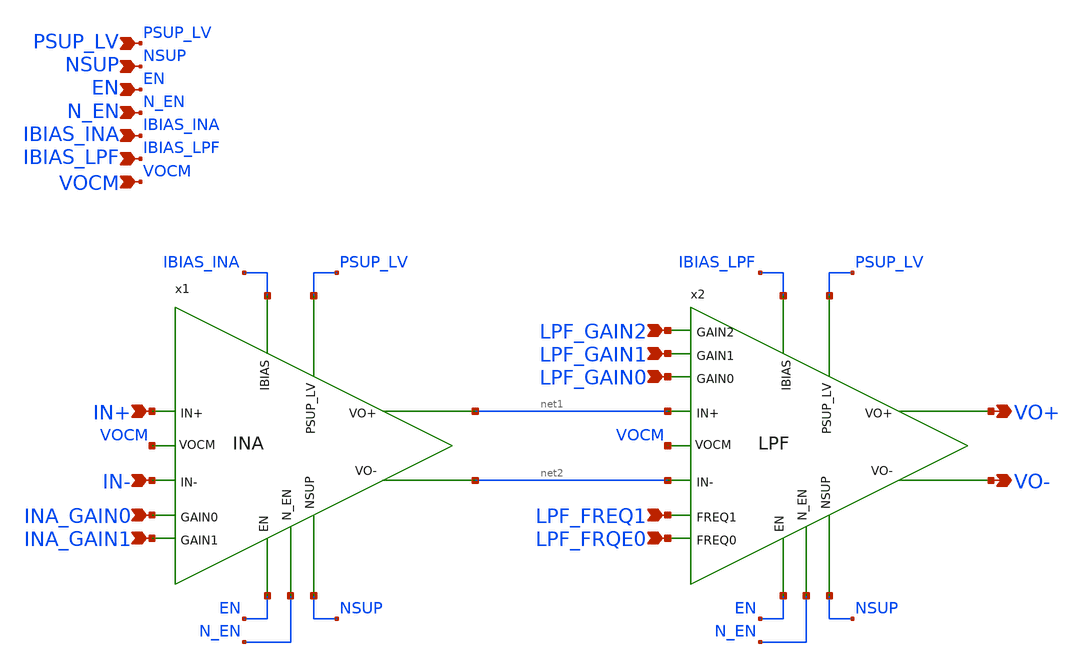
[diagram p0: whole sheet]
** sch_path: xschem/top.sch
**.subckt top IN+ IN- EN N_EN NSUP PSUP_LV IBIAS_INA VOCM VO+ VO- LPF_GAIN2 LPF_GAIN1 LPF_GAIN0
*+ LPF_FREQ1 LPF_FRQE0 INA_GAIN1 INA_GAIN0 IBIAS_LPF
*.ipin IN+
*.ipin IN-
*.ipin EN
*.ipin N_EN
*.ipin NSUP
*.ipin PSUP_LV
*.ipin IBIAS_INA
*.ipin VOCM
*.opin VO+
*.opin VO-
*.ipin LPF_GAIN2
*.ipin LPF_GAIN1
*.ipin LPF_GAIN0
*.ipin LPF_FREQ1
*.ipin LPF_FRQE0
*.ipin INA_GAIN1
*.ipin INA_GAIN0
*.ipin IBIAS_LPF
x2 PSUP_LV NSUP EN N_EN IBIAS_LPF LPF_GAIN2 LPF_GAIN1 LPF_GAIN0 LPF_FREQ1 LPF_FRQE0 net1 VO+ VOCM
+ net2 VO- LPF
x1 PSUP_LV NSUP EN N_EN IBIAS_INA INA_GAIN0 INA_GAIN1 IN+ net1 VOCM IN- net2 INA
**.ends
.end
